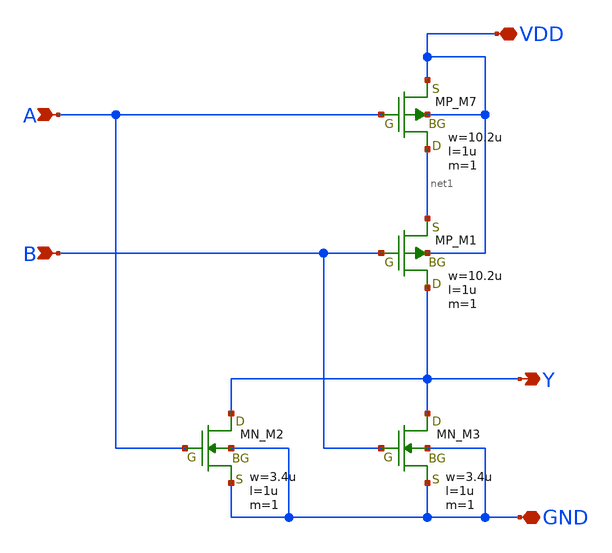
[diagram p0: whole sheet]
** sch_path: libs.tech/xschem/TR-1um_5_stdcell/NOR2.sch
**.subckt NOR2 A B Y VDD GND
*.ipin A
*.ipin B
*.opin Y
*.iopin VDD
*.iopin GND
XM7 net1 A VDD VDD PMOS w=10.2u l=1u nrd=0 nrs=0 m=1
XM1 Y B net1 VDD PMOS w=10.2u l=1u nrd=0 nrs=0 m=1
XM2 Y A GND GND NMOS w=3.4u l=1u nrd=0 nrs=0 m=1
XM3 Y B GND GND NMOS w=3.4u l=1u nrd=0 nrs=0 m=1
**.ends
.end
